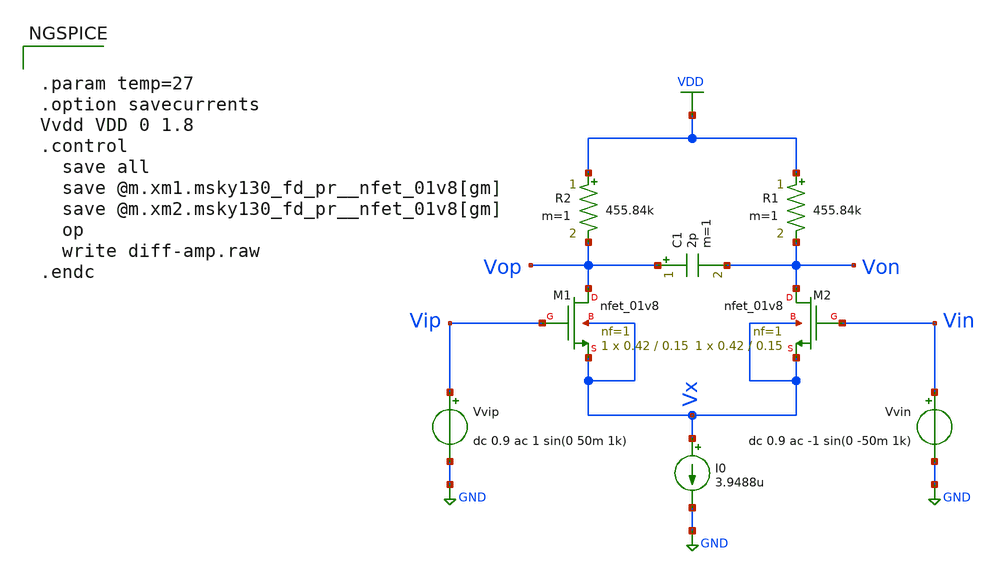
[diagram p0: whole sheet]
** sch_path: PSO/Diff-Amp/Xschem/diff-amp.sch
**.subckt diff-amp
XM1 Vop Vip Vx Vx sky130_fd_pr__nfet_01v8 L=0.15 W=0.42 nf=1 ad='int((1 + 1)/2) * 0.42 / 1 * 0.29' as='int((1 + 2)/2) * 0.42 / 1 * 0.29'
+ pd='2*int((1 + 1)/2) * (0.42 / 1 + 0.29)' ps='2*int((1 + 2)/2) * (0.42 / 1 + 0.29)' nrd='0.29 / 0.42 '
+ nrs='0.29 / 0.42 ' sa=0 sb=0 sd=0 mult=1 m=1
XM2 Von Vin Vx Vx sky130_fd_pr__nfet_01v8 L=0.15 W=0.42 nf=1 ad='int((1 + 1)/2) * 0.42 / 1 * 0.29' as='int((1 + 2)/2) * 0.42 / 1 * 0.29'
+ pd='2*int((1 + 1)/2) * (0.42 / 1 + 0.29)' ps='2*int((1 + 2)/2) * (0.42 / 1 + 0.29)' nrd='0.29 / 0.42 '
+ nrs='0.29 / 0.42 ' sa=0 sb=0 sd=0 mult=1 m=1
R1 VDD Von 455.84k m=1
R2 VDD Vop 455.84k m=1
I0 Vx GND 3.9488u
Vvip Vip GND dc 0.9 ac 1 sin(0 50m 1k)
Vvin Vin GND dc 0.9 ac -1 sin(0 -50m 1k)
C1 Vop Von 2p m=1
**** begin user architecture code

** opencircuitdesign pdks install
.lib $::SKYWATER_MODELS/sky130.lib.spice tt



.param temp=27
.option savecurrents
Vvdd VDD 0 1.8
.control
  save all
  save @m.xm1.msky130_fd_pr__nfet_01v8[gm]
  save @m.xm2.msky130_fd_pr__nfet_01v8[gm]
  op
  write diff-amp.raw
.endc




.control
  tran 1u 5m
  save all

  let v_input_diff = v(vip) - v(vin)
  let v_output_diff = v(vop) - v(von)

  plot v_input_diff v_output_diff

  meas tran v_in_pk  PP v_input_diff from=1m to=5m
  meas tran v_out_pk PP v_output_diff from=1m to=5m

  let voltage_gain = v_out_pk / v_in_pk
  print voltage_gain
.endc




.control
  alter Vvip pulse = [ 850m 950m 0 1n 1n 0.5m 1m 1 ]
  alter Vvin pulse = [ 950m 850m 0 1n 1n 0.5m 1m 1 ]
  tran 10n 520u 480u
  save all

  let v_diff = v(vop) - v(von)
  plot v_diff

  meas tran v_max FIND v_diff AT=520u
  meas tran v_min FIND v_diff AT=490u

  let v10 = v_min + 0.1*(v_max-v_min)
  let v90 = v_max - 0.1*(v_max-v_min)
  meas tran t10 WHEN v_diff=v10 RISE=1
  meas tran t90 WHEN v_diff=v90 RISE=1

  let slew_rate = ((v90 - v10) / (t90 - t10)) * 1e-6
  print slew_rate
.endc




.control
  ac dec 100 0.1 1G
  save all

  let diff_gain = (v(vop) - v(von)) / (v(vip) - v(vin))
  let db_diff_gain = db(diff_gain)
  let neg_deg_phase = 180*cph(v(von) - v(vop))/pi

  meas ac gbw_freq WHEN db_diff_gain=0 FALL=1
  let gbw_Mfreq = gbw_freq * 1e-6

  plot db_diff_gain neg_deg_phase
  print gbw_Mfreq
.endc


**** end user architecture code
**.ends
.GLOBAL GND
.GLOBAL VDD
.end
